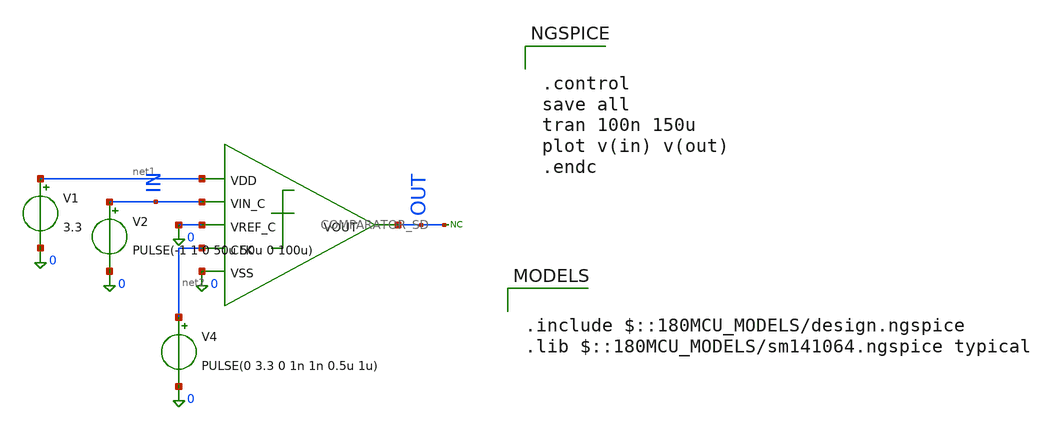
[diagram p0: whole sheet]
** sch_path: src/schematics/latched comparator/COMP_TB.sch
**.subckt COMP_TB
x1 net1 IN 0 net2 OUT 0 COMPARATOR_SD
* noconn OUT
V2 IN 0 PULSE(-1 1 0 50u 50u 0 100u)
V4 net2 0 PULSE(0 3.3 0 1n 1n 0.5u 1u)
V1 net1 0 3.3
**** begin user architecture code


.control
save all
tran 100n 150u
plot v(in) v(out)
.endc




.include $::180MCU_MODELS/design.ngspice
.lib $::180MCU_MODELS/sm141064.ngspice typical

**** end user architecture code
**.ends

* expanding   symbol:  COMPARATOR_SD.sym # of pins=6
** sym_path: src/schematics/latched comparator/COMPARATOR_SD.sym
** sch_path: src/schematics/latched comparator/COMPARATOR_SD.sch
.subckt COMPARATOR_SD VDD VIN_C VREF_C CLK VOUT VSS
*.ipin VIN_C
*.ipin VREF_C
*.ipin CLK
*.opin VOUT
*.ipin VDD
*.ipin VSS
XM5 net1 VDD VDD VDD pfet_03v3 L=0.28u W=0.22u nf=1 ad='int((nf+1)/2) * W/nf * 0.18u' as='int((nf+2)/2) * W/nf * 0.18u'
+ pd='2*int((nf+1)/2) * (W/nf + 0.18u)' ps='2*int((nf+2)/2) * (W/nf + 0.18u)' nrd='0.18u / W' nrs='0.18u / W'
+ sa=0 sb=0 sd=0 m=1
XM1 net3 VIN_C net1 net1 pfet_03v3 L=0.28u W=0.22u nf=1 ad='int((nf+1)/2) * W/nf * 0.18u' as='int((nf+2)/2) * W/nf * 0.18u'
+ pd='2*int((nf+1)/2) * (W/nf + 0.18u)' ps='2*int((nf+2)/2) * (W/nf + 0.18u)' nrd='0.18u / W' nrs='0.18u / W'
+ sa=0 sb=0 sd=0 m=1
XM2 net5 VREF_C net1 net1 pfet_03v3 L=0.28u W=0.22u nf=1 ad='int((nf+1)/2) * W/nf * 0.18u' as='int((nf+2)/2) * W/nf * 0.18u'
+ pd='2*int((nf+1)/2) * (W/nf + 0.18u)' ps='2*int((nf+2)/2) * (W/nf + 0.18u)' nrd='0.18u / W' nrs='0.18u / W'
+ sa=0 sb=0 sd=0 m=1
XM3 net4 net2 net5 net5 pfet_03v3 L=0.28u W=0.22u nf=1 ad='int((nf+1)/2) * W/nf * 0.18u' as='int((nf+2)/2) * W/nf * 0.18u'
+ pd='2*int((nf+1)/2) * (W/nf + 0.18u)' ps='2*int((nf+2)/2) * (W/nf + 0.18u)' nrd='0.18u / W' nrs='0.18u / W'
+ sa=0 sb=0 sd=0 m=1
XM4 VOUT net2 net3 net3 pfet_03v3 L=0.28u W=0.22u nf=1 ad='int((nf+1)/2) * W/nf * 0.18u' as='int((nf+2)/2) * W/nf * 0.18u'
+ pd='2*int((nf+1)/2) * (W/nf + 0.18u)' ps='2*int((nf+2)/2) * (W/nf + 0.18u)' nrd='0.18u / W' nrs='0.18u / W'
+ sa=0 sb=0 sd=0 m=1
XM6 net2 CLK VDD VDD pfet_03v3 L=0.28u W=0.22u nf=1 ad='int((nf+1)/2) * W/nf * 0.18u' as='int((nf+2)/2) * W/nf * 0.18u'
+ pd='2*int((nf+1)/2) * (W/nf + 0.18u)' ps='2*int((nf+2)/2) * (W/nf + 0.18u)' nrd='0.18u / W' nrs='0.18u / W'
+ sa=0 sb=0 sd=0 m=1
XM7 net2 CLK VSS VSS nfet_03v3 L=0.28u W=0.22u nf=1 ad='int((nf+1)/2) * W/nf * 0.18u' as='int((nf+2)/2) * W/nf * 0.18u'
+ pd='2*int((nf+1)/2) * (W/nf + 0.18u)' ps='2*int((nf+2)/2) * (W/nf + 0.18u)' nrd='0.18u / W' nrs='0.18u / W'
+ sa=0 sb=0 sd=0 m=1
XM8 VOUT CLK net4 net4 nfet_03v3 L=0.28u W=0.22u nf=1 ad='int((nf+1)/2) * W/nf * 0.18u' as='int((nf+2)/2) * W/nf * 0.18u'
+ pd='2*int((nf+1)/2) * (W/nf + 0.18u)' ps='2*int((nf+2)/2) * (W/nf + 0.18u)' nrd='0.18u / W' nrs='0.18u / W'
+ sa=0 sb=0 sd=0 m=1
XM9 net7 net4 VDD VDD pfet_03v3 L=0.28u W=0.22u nf=1 ad='int((nf+1)/2) * W/nf * 0.18u' as='int((nf+2)/2) * W/nf * 0.18u'
+ pd='2*int((nf+1)/2) * (W/nf + 0.18u)' ps='2*int((nf+2)/2) * (W/nf + 0.18u)' nrd='0.18u / W' nrs='0.18u / W'
+ sa=0 sb=0 sd=0 m=1
XM10 VOUT CLK net7 net7 pfet_03v3 L=0.28u W=0.22u nf=1 ad='int((nf+1)/2) * W/nf * 0.18u' as='int((nf+2)/2) * W/nf * 0.18u'
+ pd='2*int((nf+1)/2) * (W/nf + 0.18u)' ps='2*int((nf+2)/2) * (W/nf + 0.18u)' nrd='0.18u / W' nrs='0.18u / W'
+ sa=0 sb=0 sd=0 m=1
XM11 VOUT net4 VSS VSS nfet_03v3 L=0.28u W=0.22u nf=1 ad='int((nf+1)/2) * W/nf * 0.18u' as='int((nf+2)/2) * W/nf * 0.18u'
+ pd='2*int((nf+1)/2) * (W/nf + 0.18u)' ps='2*int((nf+2)/2) * (W/nf + 0.18u)' nrd='0.18u / W' nrs='0.18u / W'
+ sa=0 sb=0 sd=0 m=1
XM12 net6 VOUT VDD VDD pfet_03v3 L=0.28u W=0.22u nf=1 ad='int((nf+1)/2) * W/nf * 0.18u' as='int((nf+2)/2) * W/nf * 0.18u'
+ pd='2*int((nf+1)/2) * (W/nf + 0.18u)' ps='2*int((nf+2)/2) * (W/nf + 0.18u)' nrd='0.18u / W' nrs='0.18u / W'
+ sa=0 sb=0 sd=0 m=1
XM13 net4 CLK net6 net6 pfet_03v3 L=0.28u W=0.22u nf=1 ad='int((nf+1)/2) * W/nf * 0.18u' as='int((nf+2)/2) * W/nf * 0.18u'
+ pd='2*int((nf+1)/2) * (W/nf + 0.18u)' ps='2*int((nf+2)/2) * (W/nf + 0.18u)' nrd='0.18u / W' nrs='0.18u / W'
+ sa=0 sb=0 sd=0 m=1
XM14 net4 VOUT VSS VSS nfet_03v3 L=0.28u W=0.22u nf=1 ad='int((nf+1)/2) * W/nf * 0.18u' as='int((nf+2)/2) * W/nf * 0.18u'
+ pd='2*int((nf+1)/2) * (W/nf + 0.18u)' ps='2*int((nf+2)/2) * (W/nf + 0.18u)' nrd='0.18u / W' nrs='0.18u / W'
+ sa=0 sb=0 sd=0 m=1
.ends

.end
